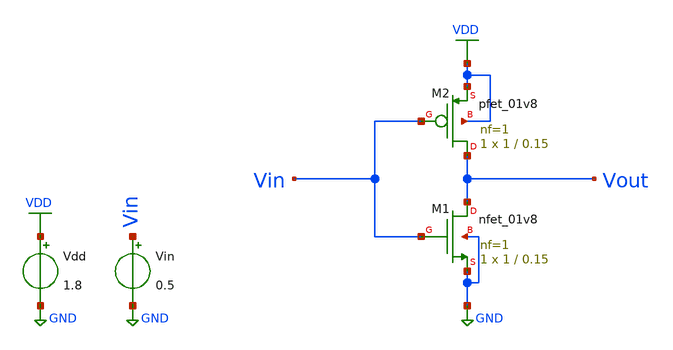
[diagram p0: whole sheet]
** sch_path: projects/montecarlo/xschem_ngspice/inverter/inverter_monte_carlo.sch
**.subckt inverter_monte_carlo
XM1 Vout Vin GND GND sky130_fd_pr__nfet_01v8 L=0.15 W=1 nf=1 ad='int((nf+1)/2) * W/nf * 0.29' as='int((nf+2)/2) * W/nf * 0.29'
+ pd='2*int((nf+1)/2) * (W/nf + 0.29)' ps='2*int((nf+2)/2) * (W/nf + 0.29)' nrd='0.29 / W' nrs='0.29 / W'
+ sa=0 sb=0 sd=0 mult=1 m=1
XM2 Vout Vin VDD VDD sky130_fd_pr__pfet_01v8 L=0.15 W=1 nf=1 ad='int((nf+1)/2) * W/nf * 0.29' as='int((nf+2)/2) * W/nf * 0.29'
+ pd='2*int((nf+1)/2) * (W/nf + 0.29)' ps='2*int((nf+2)/2) * (W/nf + 0.29)' nrd='0.29 / W' nrs='0.29 / W'
+ sa=0 sb=0 sd=0 mult=1 m=1
Vdd VDD GND 1.8
Vin Vin GND 0.5
**** begin user architecture code




.lib /foss/pdks/sky130A/libs.tech/combined/sky130.lib.spice mc
.param mc_mm_switch=1

.option wnflag=1

.control
set wr_vecnames
set wr_singlescale

let mc_runs=10
let run=1

dowhile run <= mc_runs
  dc vin 0 1.8 0.01
  wrdata /foss/designs/my_design/projects/montecarlo/xschem_ngspice/inverter{$&run}.txt v(Vout)
  reset
  let run = run + 1
end
.endc




**** end user architecture code
**.ends
.GLOBAL VDD
.GLOBAL GND
.end
